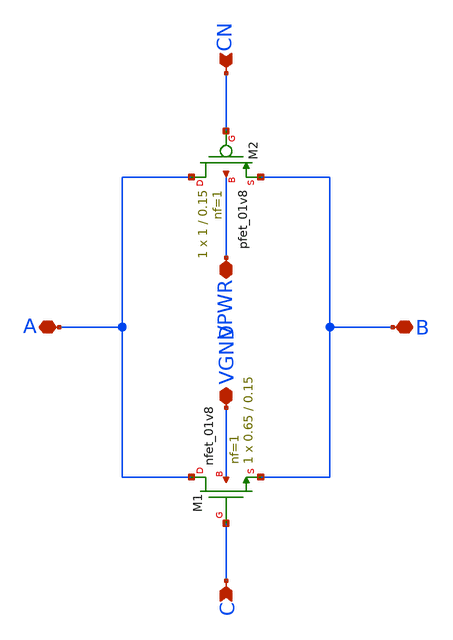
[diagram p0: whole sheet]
** sch_path: trans/tran.sch
**.subckt tran A B VPWR VGND C CN
*.iopin A
*.iopin B
*.iopin VPWR
*.iopin VGND
*.ipin C
*.ipin CN
XM1 A C B VGND sky130_fd_pr__nfet_01v8 L=0.15 W=0.65 nf=1 ad='int((1 + 1)/2) * 0.65 / 1 * 0.29' as='int((1 + 2)/2) * 0.65 / 1 * 0.29'
+ pd='2*int((1 + 1)/2) * (0.65 / 1 + 0.29)' ps='2*int((1 + 2)/2) * (0.65 / 1 + 0.29)' nrd='0.29 / 0.65 '
+ nrs='0.29 / 0.65 ' sa=0 sb=0 sd=0 mult=1 m=1
XM2 A CN B VPWR sky130_fd_pr__pfet_01v8 L=0.15 W=1 nf=1 ad='int((1 + 1)/2) * 1 / 1 * 0.29' as='int((1 + 2)/2) * 1 / 1 * 0.29'
+ pd='2*int((1 + 1)/2) * (1 / 1 + 0.29)' ps='2*int((1 + 2)/2) * (1 / 1 + 0.29)' nrd='0.29 / 1 ' nrs='0.29 / 1 '
+ sa=0 sb=0 sd=0 mult=1 m=1
**.ends
.end
